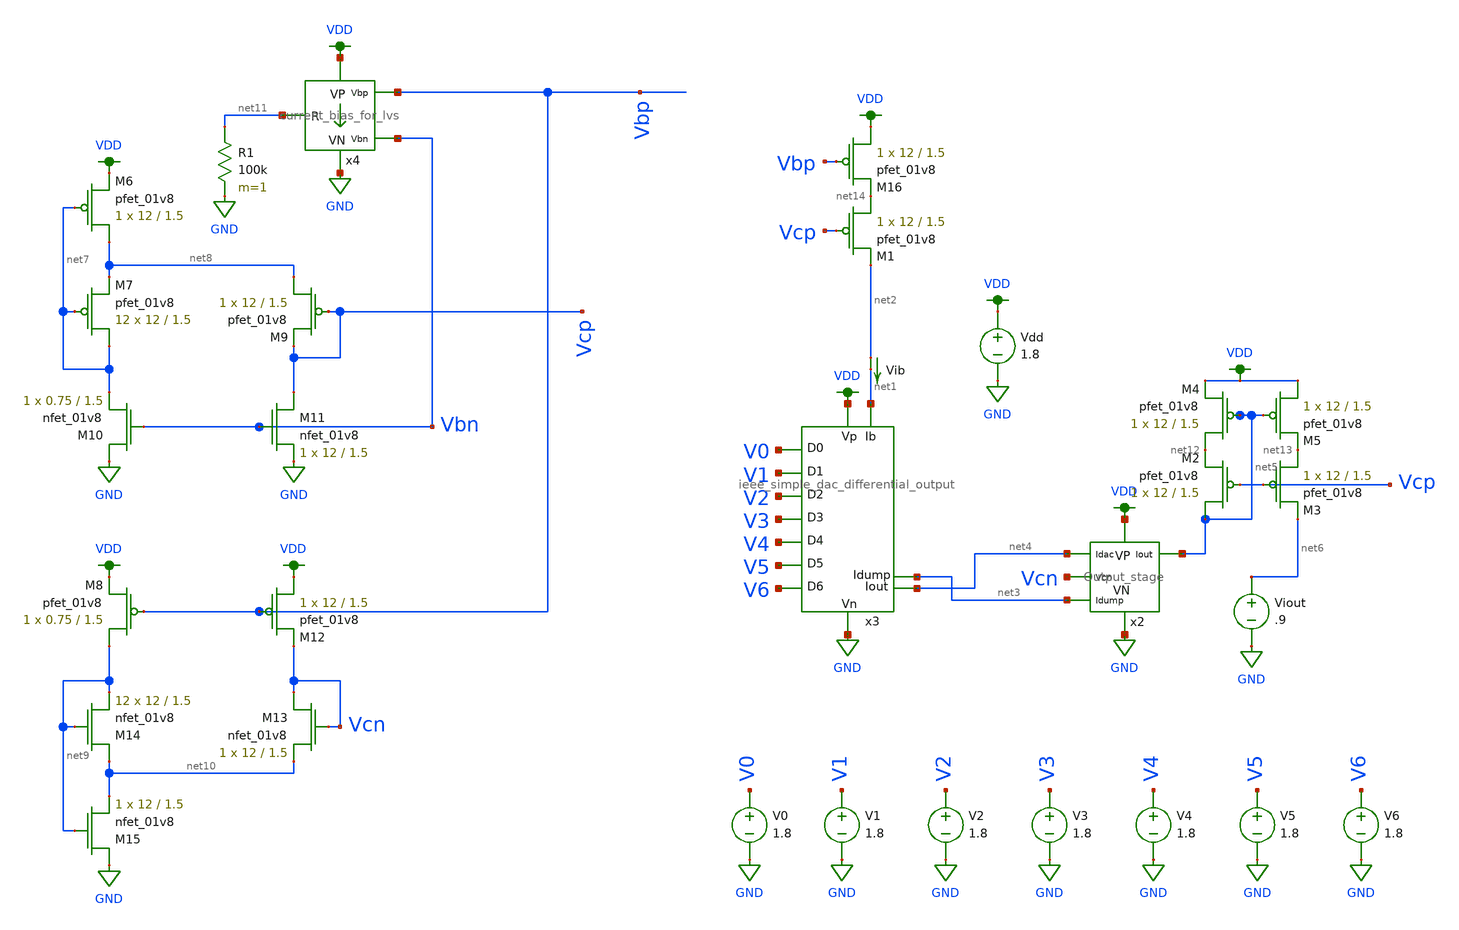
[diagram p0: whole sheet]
** sch_path: schematics/ieee DAC/ieee_DAC_mc_simulation_70.sch
**.subckt ieee_DAC_mc_simulation_70
Vdd VDD GND 1.8
V1 V1 GND 1.8
V2 V2 GND 1.8
V3 V3 GND 1.8
V4 V4 GND 1.8
V5 V5 GND 1.8
V6 V6 GND 1.8
V0 V0 GND 1.8
Vib net2 net1 0
.save i(vib)
x2 VDD GND net5 Vcn net4 net3 Output_stage
x3 VDD net3 GND V1 V0 V2 V3 V4 V5 V6 net1 net4 ieee_simple_dac_differential_output
Viout net6 GND .9
XM2 net5 Vcp net12 VDD sky130_fd_pr__pfet_01v8 L=1.5 W=12 nf=1 ad='int((nf+1)/2) * W/nf * 0.29' as='int((nf+2)/2) * W/nf * 0.29'
+ pd='2*int((nf+1)/2) * (W/nf + 0.29)' ps='2*int((nf+2)/2) * (W/nf + 0.29)' nrd='0.29 / W' nrs='0.29 / W'
+ sa=0 sb=0 sd=0 mult=1 m=1
XM3 net13 Vcp net6 VDD sky130_fd_pr__pfet_01v8 L=1.5 W=12 nf=1 ad='int((nf+1)/2) * W/nf * 0.29' as='int((nf+2)/2) * W/nf * 0.29'
+ pd='2*int((nf+1)/2) * (W/nf + 0.29)' ps='2*int((nf+2)/2) * (W/nf + 0.29)' nrd='0.29 / W' nrs='0.29 / W'
+ sa=0 sb=0 sd=0 mult=1 m=1
XM4 net12 net5 VDD VDD sky130_fd_pr__pfet_01v8 L=1.5 W=12 nf=1 ad='int((nf+1)/2) * W/nf * 0.29' as='int((nf+2)/2) * W/nf * 0.29'
+ pd='2*int((nf+1)/2) * (W/nf + 0.29)' ps='2*int((nf+2)/2) * (W/nf + 0.29)' nrd='0.29 / W' nrs='0.29 / W'
+ sa=0 sb=0 sd=0 mult=1 m=1
XM5 VDD net5 net13 VDD sky130_fd_pr__pfet_01v8 L=1.5 W=12 nf=1 ad='int((nf+1)/2) * W/nf * 0.29' as='int((nf+2)/2) * W/nf * 0.29'
+ pd='2*int((nf+1)/2) * (W/nf + 0.29)' ps='2*int((nf+2)/2) * (W/nf + 0.29)' nrd='0.29 / W' nrs='0.29 / W'
+ sa=0 sb=0 sd=0 mult=1 m=1
XM6 net8 net7 VDD VDD sky130_fd_pr__pfet_01v8 L=1.5 W=12 nf=1 ad='int((nf+1)/2) * W/nf * 0.29' as='int((nf+2)/2) * W/nf * 0.29'
+ pd='2*int((nf+1)/2) * (W/nf + 0.29)' ps='2*int((nf+2)/2) * (W/nf + 0.29)' nrd='0.29 / W' nrs='0.29 / W'
+ sa=0 sb=0 sd=0 mult=1 m=1
XM7 net7 net7 net8 VDD sky130_fd_pr__pfet_01v8 L=1.5 W=12 nf=1 ad='int((nf+1)/2) * W/nf * 0.29' as='int((nf+2)/2) * W/nf * 0.29'
+ pd='2*int((nf+1)/2) * (W/nf + 0.29)' ps='2*int((nf+2)/2) * (W/nf + 0.29)' nrd='0.29 / W' nrs='0.29 / W'
+ sa=0 sb=0 sd=0 mult=12 m=12
XM9 net8 Vcp Vcp VDD sky130_fd_pr__pfet_01v8 L=1.5 W=12 nf=1 ad='int((nf+1)/2) * W/nf * 0.29' as='int((nf+2)/2) * W/nf * 0.29'
+ pd='2*int((nf+1)/2) * (W/nf + 0.29)' ps='2*int((nf+2)/2) * (W/nf + 0.29)' nrd='0.29 / W' nrs='0.29 / W'
+ sa=0 sb=0 sd=0 mult=1 m=1
XM10 GND Vbn net7 GND sky130_fd_pr__nfet_01v8 L=1.5 W=0.75 nf=1 ad='int((nf+1)/2) * W/nf * 0.29' as='int((nf+2)/2) * W/nf * 0.29'
+ pd='2*int((nf+1)/2) * (W/nf + 0.29)' ps='2*int((nf+2)/2) * (W/nf + 0.29)' nrd='0.29 / W' nrs='0.29 / W'
+ sa=0 sb=0 sd=0 mult=1 m=1
XM11 Vcp Vbn GND GND sky130_fd_pr__nfet_01v8 L=1.5 W=12 nf=1 ad='int((nf+1)/2) * W/nf * 0.29' as='int((nf+2)/2) * W/nf * 0.29'
+ pd='2*int((nf+1)/2) * (W/nf + 0.29)' ps='2*int((nf+2)/2) * (W/nf + 0.29)' nrd='0.29 / W' nrs='0.29 / W'
+ sa=0 sb=0 sd=0 mult=1 m=1
XM8 net9 Vbp VDD VDD sky130_fd_pr__pfet_01v8 L=1.5 W=0.75 nf=1 ad='int((nf+1)/2) * W/nf * 0.29' as='int((nf+2)/2) * W/nf * 0.29'
+ pd='2*int((nf+1)/2) * (W/nf + 0.29)' ps='2*int((nf+2)/2) * (W/nf + 0.29)' nrd='0.29 / W' nrs='0.29 / W'
+ sa=0 sb=0 sd=0 mult=1 m=1
XM12 VDD Vbp Vcn VDD sky130_fd_pr__pfet_01v8 L=1.5 W=12 nf=1 ad='int((nf+1)/2) * W/nf * 0.29' as='int((nf+2)/2) * W/nf * 0.29'
+ pd='2*int((nf+1)/2) * (W/nf + 0.29)' ps='2*int((nf+2)/2) * (W/nf + 0.29)' nrd='0.29 / W' nrs='0.29 / W'
+ sa=0 sb=0 sd=0 mult=1 m=1
XM13 Vcn Vcn net10 GND sky130_fd_pr__nfet_01v8 L=1.5 W=12 nf=1 ad='int((nf+1)/2) * W/nf * 0.29' as='int((nf+2)/2) * W/nf * 0.29'
+ pd='2*int((nf+1)/2) * (W/nf + 0.29)' ps='2*int((nf+2)/2) * (W/nf + 0.29)' nrd='0.29 / W' nrs='0.29 / W'
+ sa=0 sb=0 sd=0 mult=1 m=1
XM14 net10 net9 net9 GND sky130_fd_pr__nfet_01v8 L=1.5 W=12 nf=1 ad='int((nf+1)/2) * W/nf * 0.29' as='int((nf+2)/2) * W/nf * 0.29'
+ pd='2*int((nf+1)/2) * (W/nf + 0.29)' ps='2*int((nf+2)/2) * (W/nf + 0.29)' nrd='0.29 / W' nrs='0.29 / W'
+ sa=0 sb=0 sd=0 mult=12 m=12
XM15 GND net9 net10 GND sky130_fd_pr__nfet_01v8 L=1.5 W=12 nf=1 ad='int((nf+1)/2) * W/nf * 0.29' as='int((nf+2)/2) * W/nf * 0.29'
+ pd='2*int((nf+1)/2) * (W/nf + 0.29)' ps='2*int((nf+2)/2) * (W/nf + 0.29)' nrd='0.29 / W' nrs='0.29 / W'
+ sa=0 sb=0 sd=0 mult=1 m=1
XM1 net14 Vcp net2 VDD sky130_fd_pr__pfet_01v8 L=1.5 W=12 nf=1 ad='int((nf+1)/2) * W/nf * 0.29' as='int((nf+2)/2) * W/nf * 0.29'
+ pd='2*int((nf+1)/2) * (W/nf + 0.29)' ps='2*int((nf+2)/2) * (W/nf + 0.29)' nrd='0.29 / W' nrs='0.29 / W'
+ sa=0 sb=0 sd=0 mult=1 m=1
XM16 VDD Vbp net14 VDD sky130_fd_pr__pfet_01v8 L=1.5 W=12 nf=1 ad='int((nf+1)/2) * W/nf * 0.29' as='int((nf+2)/2) * W/nf * 0.29'
+ pd='2*int((nf+1)/2) * (W/nf + 0.29)' ps='2*int((nf+2)/2) * (W/nf + 0.29)' nrd='0.29 / W' nrs='0.29 / W'
+ sa=0 sb=0 sd=0 mult=1 m=1
R1 net11 GND 100k m=1
x4 VDD GND Vbp Vbn net11 current_bias_for_lvs
**** begin user architecture code

.option wnflag=1
.param MC_SWITCH=0.0
.lib ~/skywater/skywater-pdk/libraries/sky130_fd_pr_ngspice/latest/models/sky130.lib.spice tt


.save all
.control
set wr_vecnames
set wr_singlescale

let Ibias_max = 31n
let Ibias = 30n
dowhile Ibias < Ibias_max
alter Ib $&Ibias

let mc_runs = 1
let run = 1
dowhile run <= mc_runs

  let code = 0
  while code < 128
    if floor(code / 1) eq 0
      let b0 = 0
    else
      let b0 = (floor(code / 1) % 2) * 1.8
    end
    if floor(code / 2) eq 0
      let b1 = 0
    else
      let b1 = (floor(code / 2) % 2) * 1.8
    end
    if floor(code / 4) eq 0
      let b2 = 0
    else
      let b2 = (floor(code / 4) % 2) * 1.8
    end
    if floor(code / 8) eq 0
      let b3 = 0
    else
      let b3 = (floor(code / 8) % 2) * 1.8
    end
    if floor(code / 16) eq 0
      let b4 = 0
    else
      let b4 = (floor(code / 16) % 2) * 1.8
    end
    if floor(code / 32) eq 0
      let b5 = 0
    else
      let b5 = (floor(code / 32) % 2) * 1.8
    end
    if floor(code / 64) eq 0
      let b6 = 0
    else
      let b6 = (floor(code / 64) % 2) * 1.8
    end

    alter V0 $&b0
    alter V1 $&b1
    alter V2 $&b2
    alter V3 $&b3
    alter V4 $&b4
    alter V5 $&b5
    alter V6 $&b6
    save all
    op

    wrdata ~/dev/git/7-bit-D-A-converter-MP4-MADVLSI/schematics/simulations/ieee_DAC/dac_with_external_bias_gen/test_71/ieeeDAC_{$&run}.txt
+ V0 V1 V2 V3 V4 V5 V6 i(Vib) i(Viout)
    if code eq 0
      set appendwrite
      set wr_vecnames = FALSE
    end
    let code = code + 1
  end
  reset
  set appendwrite = FALSE
  set wr_vecnames
  let run = run + 1
end

let Ibias = Ibias * 2
end
.endc

**** end user architecture code
**.ends
.GLOBAL VDD
.GLOBAL GND
.end
